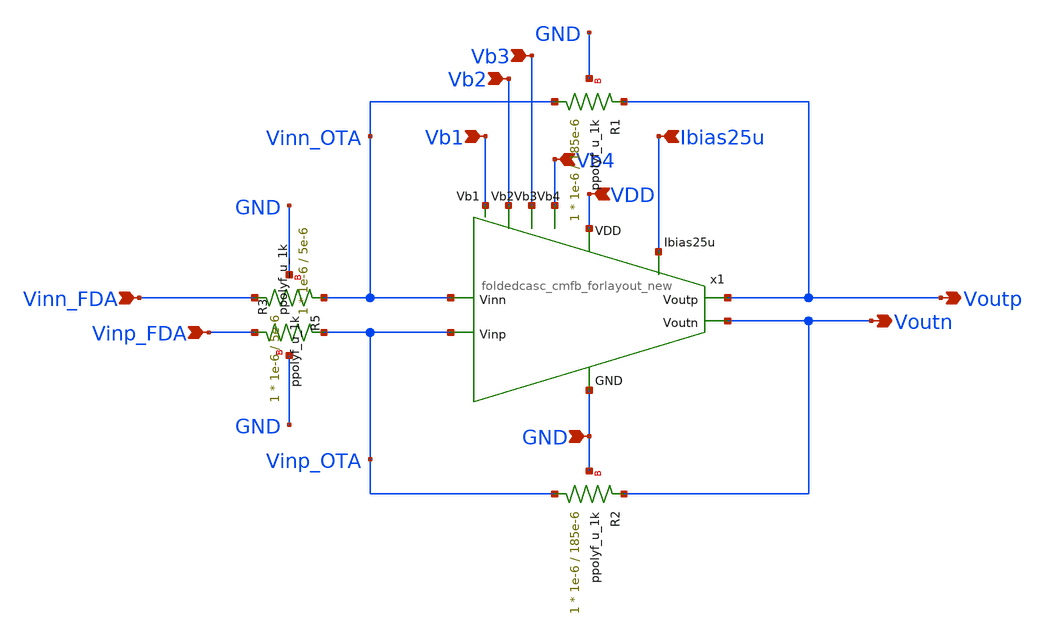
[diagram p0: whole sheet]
** sch_path: jz_fda2/xschem/fda2_forlayout_new.sch
**.subckt fda2_forlayout_new Vinn_FDA Voutp Voutn Vinp_FDA Vb1 Vb2 Vb3 Vb4 VDD Ibias25u GND
*.ipin Vinn_FDA
*.opin Voutp
*.opin Voutn
*.ipin Vinp_FDA
*.ipin Vb1
*.ipin Vb2
*.ipin Vb3
*.ipin Vb4
*.ipin VDD
*.ipin Ibias25u
*.ipin GND
XR5 Vinn_FDA Vinn_OTA GND ppolyf_u_1k r_width=1e-6 r_length=5e-6 m=1
XR3 Vinp_OTA Vinp_FDA GND ppolyf_u_1k r_width=1e-6 r_length=5e-6 m=1
XR1 Vinn_OTA Voutp GND ppolyf_u_1k r_width=1e-6 r_length=185e-6 m=1
XR2 Vinp_OTA Voutn GND ppolyf_u_1k r_width=1e-6 r_length=185e-6 m=1
x1 VDD Vb2 Voutp Voutn Vb1 Ibias25u Vinn_OTA GND Vinp_OTA Vb3 Vb4 foldedcasc_cmfb_forlayout_new
**.ends

* expanding   symbol:  chipathon-2026-ppg/jz_fda2/xschem/foldedcasc_cmfb_forlayout_new.sym # of
*+ pins=11
** sym_path: jz_fda2/xschem/foldedcasc_cmfb_forlayout_new.sym
** sch_path: jz_fda2/xschem/foldedcasc_cmfb_forlayout_new.sch
.subckt foldedcasc_cmfb_forlayout_new VDD Vb2 Voutp Voutn Vb1 Ibias25u Vinn GND Vinp Vb3 Vb4
*.ipin VDD
*.opin Voutp
*.ipin Vinn
*.ipin Ibias25u
*.ipin GND
*.ipin Vinp
*.opin Voutn
*.ipin Vb4
*.ipin Vb1
*.ipin Vb2
*.ipin Vb3
XM5 net1 Vb3 GND GND nfet_03v3 L=0.56u W=26u nf=4 ad='int((nf+1)/2) * W/nf * 0.18u' as='int((nf+2)/2) * W/nf * 0.18u'
+ pd='2*int((nf+1)/2) * (W/nf + 0.18u)' ps='2*int((nf+2)/2) * (W/nf + 0.18u)' nrd='0.18u / W' nrs='0.18u / W'
+ sa=0 sb=0 sd=0 m=1
XM6 Voutn Vb2 net2 GND nfet_03v3 L=0.56u W=35u nf=2 ad='int((nf+1)/2) * W/nf * 0.18u' as='int((nf+2)/2) * W/nf * 0.18u'
+ pd='2*int((nf+1)/2) * (W/nf + 0.18u)' ps='2*int((nf+2)/2) * (W/nf + 0.18u)' nrd='0.18u / W' nrs='0.18u / W'
+ sa=0 sb=0 sd=0 m=1
XM7 Voutp Vb2 net1 GND nfet_03v3 L=0.56u W=35u nf=2 ad='int((nf+1)/2) * W/nf * 0.18u' as='int((nf+2)/2) * W/nf * 0.18u'
+ pd='2*int((nf+1)/2) * (W/nf + 0.18u)' ps='2*int((nf+2)/2) * (W/nf + 0.18u)' nrd='0.18u / W' nrs='0.18u / W'
+ sa=0 sb=0 sd=0 m=1
XM8 Voutn Vb1 net3 VDD pfet_03v3 L=0.56u W=24u nf=5 ad='int((nf+1)/2) * W/nf * 0.18u' as='int((nf+2)/2) * W/nf * 0.18u'
+ pd='2*int((nf+1)/2) * (W/nf + 0.18u)' ps='2*int((nf+2)/2) * (W/nf + 0.18u)' nrd='0.18u / W' nrs='0.18u / W'
+ sa=0 sb=0 sd=0 m=1
XM9 Voutp Vb1 net4 VDD pfet_03v3 L=0.56u W=24u nf=5 ad='int((nf+1)/2) * W/nf * 0.18u' as='int((nf+2)/2) * W/nf * 0.18u'
+ pd='2*int((nf+1)/2) * (W/nf + 0.18u)' ps='2*int((nf+2)/2) * (W/nf + 0.18u)' nrd='0.18u / W' nrs='0.18u / W'
+ sa=0 sb=0 sd=0 m=1
XM10 net3 Vb4 VDD VDD pfet_03v3 L=0.56u W=23u nf=4 ad='int((nf+1)/2) * W/nf * 0.18u' as='int((nf+2)/2) * W/nf * 0.18u'
+ pd='2*int((nf+1)/2) * (W/nf + 0.18u)' ps='2*int((nf+2)/2) * (W/nf + 0.18u)' nrd='0.18u / W' nrs='0.18u / W'
+ sa=0 sb=0 sd=0 m=1
XM11 net4 Vb4 VDD VDD pfet_03v3 L=0.56u W=23u nf=4 ad='int((nf+1)/2) * W/nf * 0.18u' as='int((nf+2)/2) * W/nf * 0.18u'
+ pd='2*int((nf+1)/2) * (W/nf + 0.18u)' ps='2*int((nf+2)/2) * (W/nf + 0.18u)' nrd='0.18u / W' nrs='0.18u / W'
+ sa=0 sb=0 sd=0 m=1
XM1 net1 Vinn net5 VDD pfet_03v3 L=0.28u W=3.45u nf=1 ad='int((nf+1)/2) * W/nf * 0.18u' as='int((nf+2)/2) * W/nf * 0.18u'
+ pd='2*int((nf+1)/2) * (W/nf + 0.18u)' ps='2*int((nf+2)/2) * (W/nf + 0.18u)' nrd='0.18u / W' nrs='0.18u / W'
+ sa=0 sb=0 sd=0 m=1
XM2 net2 Vinp net5 VDD pfet_03v3 L=0.28u W=3.45u nf=1 ad='int((nf+1)/2) * W/nf * 0.18u' as='int((nf+2)/2) * W/nf * 0.18u'
+ pd='2*int((nf+1)/2) * (W/nf + 0.18u)' ps='2*int((nf+2)/2) * (W/nf + 0.18u)' nrd='0.18u / W' nrs='0.18u / W'
+ sa=0 sb=0 sd=0 m=1
XM3 net5 Ibias25u net6 VDD pfet_03v3 L=0.28u W=4.9u nf=2 ad='int((nf+1)/2) * W/nf * 0.18u' as='int((nf+2)/2) * W/nf * 0.18u'
+ pd='2*int((nf+1)/2) * (W/nf + 0.18u)' ps='2*int((nf+2)/2) * (W/nf + 0.18u)' nrd='0.18u / W' nrs='0.18u / W'
+ sa=0 sb=0 sd=0 m=1
XM12 Ibias25u Ibias25u VDD VDD pfet_03v3 L=0.28u W=2.27u nf=1 ad='int((nf+1)/2) * W/nf * 0.18u' as='int((nf+2)/2) * W/nf * 0.18u'
+ pd='2*int((nf+1)/2) * (W/nf + 0.18u)' ps='2*int((nf+2)/2) * (W/nf + 0.18u)' nrd='0.18u / W' nrs='0.18u / W'
+ sa=0 sb=0 sd=0 m=1
XM13 net6 Voutp VDD VDD pfet_03v3 L=0.28u W=30u nf=3 ad='int((nf+1)/2) * W/nf * 0.18u' as='int((nf+2)/2) * W/nf * 0.18u'
+ pd='2*int((nf+1)/2) * (W/nf + 0.18u)' ps='2*int((nf+2)/2) * (W/nf + 0.18u)' nrd='0.18u / W' nrs='0.18u / W'
+ sa=0 sb=0 sd=0 m=1
XM14 net6 Voutn VDD VDD pfet_03v3 L=0.28u W=30u nf=3 ad='int((nf+1)/2) * W/nf * 0.18u' as='int((nf+2)/2) * W/nf * 0.18u'
+ pd='2*int((nf+1)/2) * (W/nf + 0.18u)' ps='2*int((nf+2)/2) * (W/nf + 0.18u)' nrd='0.18u / W' nrs='0.18u / W'
+ sa=0 sb=0 sd=0 m=1
XM4 net2 Vb3 GND GND nfet_03v3 L=0.56u W=26u nf=4 ad='int((nf+1)/2) * W/nf * 0.18u' as='int((nf+2)/2) * W/nf * 0.18u'
+ pd='2*int((nf+1)/2) * (W/nf + 0.18u)' ps='2*int((nf+2)/2) * (W/nf + 0.18u)' nrd='0.18u / W' nrs='0.18u / W'
+ sa=0 sb=0 sd=0 m=1
XM15 VDD VDD VDD VDD pfet_03v3 L=0.28u W=2.27u nf=1 ad='int((nf+1)/2) * W/nf * 0.18u' as='int((nf+2)/2) * W/nf * 0.18u'
+ pd='2*int((nf+1)/2) * (W/nf + 0.18u)' ps='2*int((nf+2)/2) * (W/nf + 0.18u)' nrd='0.18u / W' nrs='0.18u / W'
+ sa=0 sb=0 sd=0 m=1
.ends

.end
